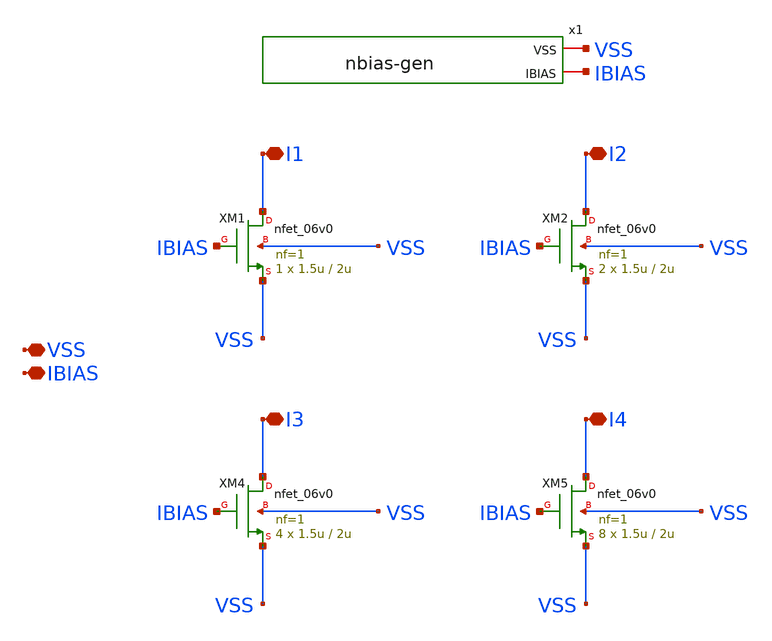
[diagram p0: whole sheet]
** sch_path: designs/libs/core_current-mirror/nmos_current_mirror/nmos_current_mirror.sch
**.subckt nmos_current_mirror VSS IBIAS I1 I2 I4 I3
*.iopin VSS
*.iopin IBIAS
*.iopin I1
*.iopin I2
*.iopin I4
*.iopin I3
x1 VSS IBIAS nbias-gen
XM1 I1 IBIAS VSS VSS nfet_06v0 L=2u W=1.5u nf=1 ad='int((nf+1)/2) * W/nf * 0.18u' as='int((nf+2)/2) * W/nf * 0.18u'
+ pd='2*int((nf+1)/2) * (W/nf + 0.18u)' ps='2*int((nf+2)/2) * (W/nf + 0.18u)' nrd='0.18u / W' nrs='0.18u / W'
+ sa=0 sb=0 sd=0 m=1
XM2 I2 IBIAS VSS VSS nfet_06v0 L=2u W=1.5u nf=1 ad='int((nf+1)/2) * W/nf * 0.18u' as='int((nf+2)/2) * W/nf * 0.18u'
+ pd='2*int((nf+1)/2) * (W/nf + 0.18u)' ps='2*int((nf+2)/2) * (W/nf + 0.18u)' nrd='0.18u / W' nrs='0.18u / W'
+ sa=0 sb=0 sd=0 m=2
XM4 I3 IBIAS VSS VSS nfet_06v0 L=2u W=1.5u nf=1 ad='int((nf+1)/2) * W/nf * 0.18u' as='int((nf+2)/2) * W/nf * 0.18u'
+ pd='2*int((nf+1)/2) * (W/nf + 0.18u)' ps='2*int((nf+2)/2) * (W/nf + 0.18u)' nrd='0.18u / W' nrs='0.18u / W'
+ sa=0 sb=0 sd=0 m=4
XM5 I4 IBIAS VSS VSS nfet_06v0 L=2u W=1.5u nf=1 ad='int((nf+1)/2) * W/nf * 0.18u' as='int((nf+2)/2) * W/nf * 0.18u'
+ pd='2*int((nf+1)/2) * (W/nf + 0.18u)' ps='2*int((nf+2)/2) * (W/nf + 0.18u)' nrd='0.18u / W' nrs='0.18u / W'
+ sa=0 sb=0 sd=0 m=8
**.ends

* expanding   symbol:  libs/core_current-mirror/nbias-gen/nbias-gen.sym # of pins=2
** sym_path: designs/libs/core_current-mirror/nbias-gen/nbias-gen.sym
** sch_path: designs/libs/core_current-mirror/nbias-gen/nbias-gen.sch
.subckt nbias-gen VSS IBIAS
*.iopin VSS
*.iopin IBIAS
XM1 IBIAS IBIAS VSS VSS nfet_06v0 L=2u W=1.5u nf=1 ad='int((nf+1)/2) * W/nf * 0.18u' as='int((nf+2)/2) * W/nf * 0.18u'
+ pd='2*int((nf+1)/2) * (W/nf + 0.18u)' ps='2*int((nf+2)/2) * (W/nf + 0.18u)' nrd='0.18u / W' nrs='0.18u / W'
+ sa=0 sb=0 sd=0 m=1
.ends

.end
